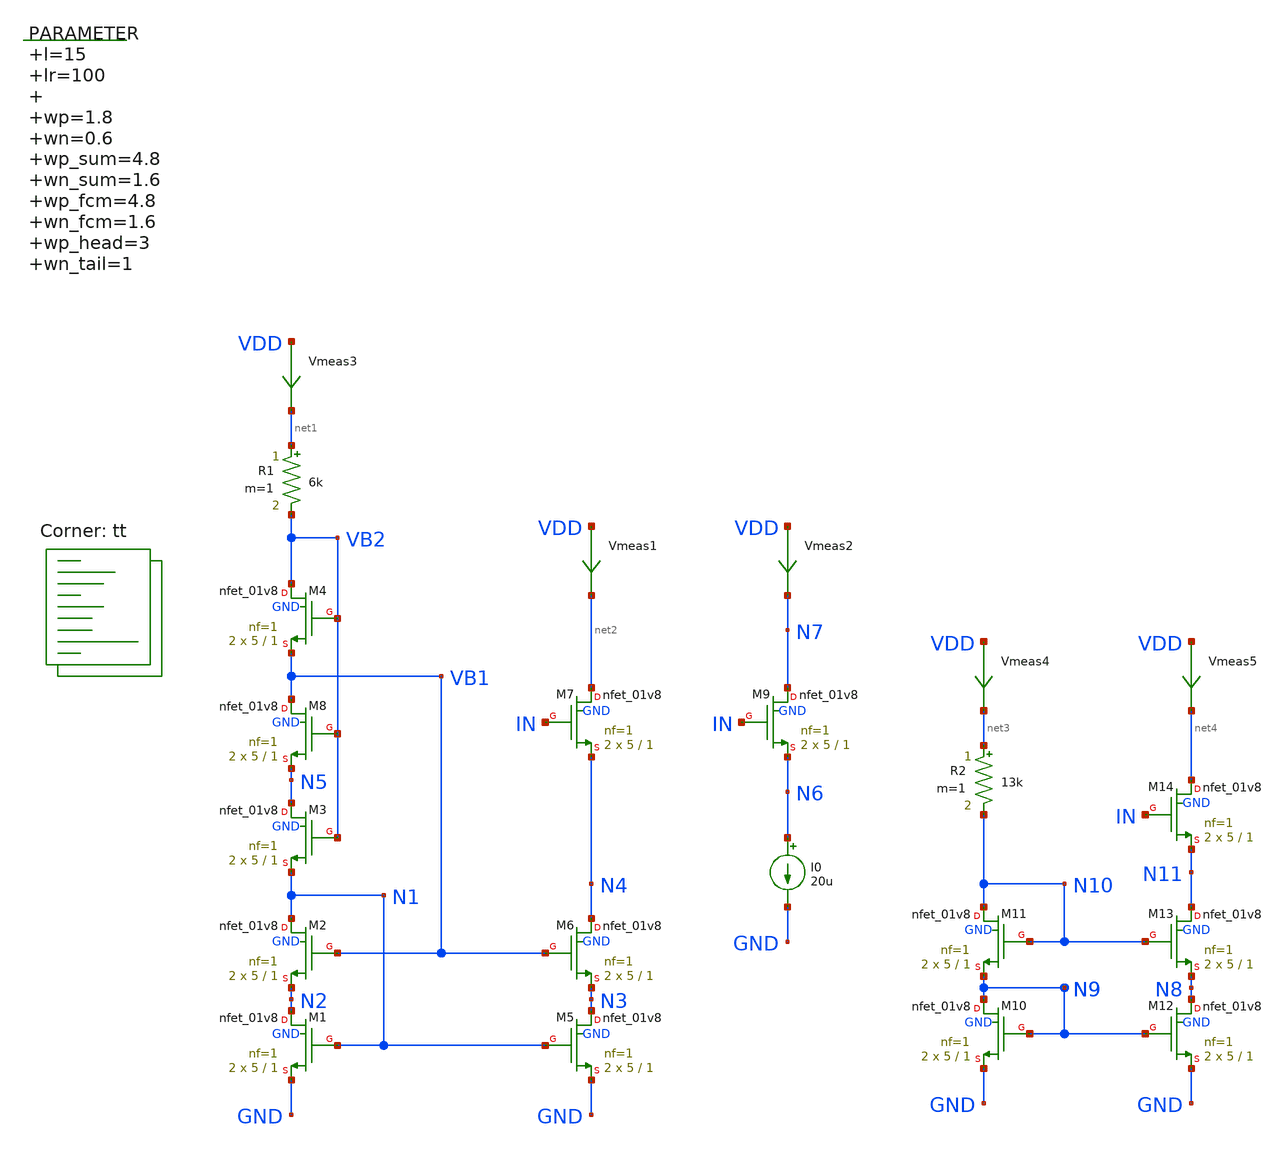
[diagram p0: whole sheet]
** sch_path: xschem/current_mirror_characterization2-tb.sch
**.subckt current_mirror_characterization2-tb
.param l=15 lr=100 wp=1.8 wn=0.6 wp_sum=4.8 wn_sum=1.6 wp_fcm=4.8 wn_fcm=1.6 wp_head=3 wn_tail=1
+ wp_bsum=4.8 wn_bsum=1.6 m=10 m1=5 m_sum=2 m_refsum=5 m_fcm=2 mdiff0=2
Vmeas3 VDD net1 0
.save i(vmeas3)
XM1 N2 N1 GND GND sky130_fd_pr__nfet_01v8 L=1 W=5 nf=1 ad='int((nf+1)/2) * W/nf * 0.29' as='int((nf+2)/2) * W/nf * 0.29'
+ pd='2*int((nf+1)/2) * (W/nf + 0.29)' ps='2*int((nf+2)/2) * (W/nf + 0.29)' nrd='0.29 / W' nrs='0.29 / W'
+ sa=0 sb=0 sd=0 mult=2 m=2
R1 net1 VB2 6k m=1
XM2 N1 VB1 N2 GND sky130_fd_pr__nfet_01v8 L=1 W=5 nf=1 ad='int((nf+1)/2) * W/nf * 0.29' as='int((nf+2)/2) * W/nf * 0.29'
+ pd='2*int((nf+1)/2) * (W/nf + 0.29)' ps='2*int((nf+2)/2) * (W/nf + 0.29)' nrd='0.29 / W' nrs='0.29 / W'
+ sa=0 sb=0 sd=0 mult=2 m=2
XM3 N5 VB2 N1 GND sky130_fd_pr__nfet_01v8 L=1 W=5 nf=1 ad='int((nf+1)/2) * W/nf * 0.29' as='int((nf+2)/2) * W/nf * 0.29'
+ pd='2*int((nf+1)/2) * (W/nf + 0.29)' ps='2*int((nf+2)/2) * (W/nf + 0.29)' nrd='0.29 / W' nrs='0.29 / W'
+ sa=0 sb=0 sd=0 mult=2 m=2
XM4 VB2 VB2 VB1 GND sky130_fd_pr__nfet_01v8 L=1 W=5 nf=1 ad='int((nf+1)/2) * W/nf * 0.29' as='int((nf+2)/2) * W/nf * 0.29'
+ pd='2*int((nf+1)/2) * (W/nf + 0.29)' ps='2*int((nf+2)/2) * (W/nf + 0.29)' nrd='0.29 / W' nrs='0.29 / W'
+ sa=0 sb=0 sd=0 mult=2 m=2
XM5 N3 N1 GND GND sky130_fd_pr__nfet_01v8 L=1 W=5 nf=1 ad='int((nf+1)/2) * W/nf * 0.29' as='int((nf+2)/2) * W/nf * 0.29'
+ pd='2*int((nf+1)/2) * (W/nf + 0.29)' ps='2*int((nf+2)/2) * (W/nf + 0.29)' nrd='0.29 / W' nrs='0.29 / W'
+ sa=0 sb=0 sd=0 mult=2 m=2
XM6 N4 VB1 N3 GND sky130_fd_pr__nfet_01v8 L=1 W=5 nf=1 ad='int((nf+1)/2) * W/nf * 0.29' as='int((nf+2)/2) * W/nf * 0.29'
+ pd='2*int((nf+1)/2) * (W/nf + 0.29)' ps='2*int((nf+2)/2) * (W/nf + 0.29)' nrd='0.29 / W' nrs='0.29 / W'
+ sa=0 sb=0 sd=0 mult=2 m=2
Vmeas1 VDD net2 0
.save i(vmeas1)
XM8 VB1 VB2 N5 GND sky130_fd_pr__nfet_01v8 L=1 W=5 nf=1 ad='int((nf+1)/2) * W/nf * 0.29' as='int((nf+2)/2) * W/nf * 0.29'
+ pd='2*int((nf+1)/2) * (W/nf + 0.29)' ps='2*int((nf+2)/2) * (W/nf + 0.29)' nrd='0.29 / W' nrs='0.29 / W'
+ sa=0 sb=0 sd=0 mult=2 m=2
XM7 net2 IN N4 GND sky130_fd_pr__nfet_01v8 L=1 W=5 nf=1 ad='int((nf+1)/2) * W/nf * 0.29' as='int((nf+2)/2) * W/nf * 0.29'
+ pd='2*int((nf+1)/2) * (W/nf + 0.29)' ps='2*int((nf+2)/2) * (W/nf + 0.29)' nrd='0.29 / W' nrs='0.29 / W'
+ sa=0 sb=0 sd=0 mult=2 m=2
Vmeas2 VDD N7 0
.save i(vmeas2)
XM9 N7 IN N6 GND sky130_fd_pr__nfet_01v8 L=1 W=5 nf=1 ad='int((nf+1)/2) * W/nf * 0.29' as='int((nf+2)/2) * W/nf * 0.29'
+ pd='2*int((nf+1)/2) * (W/nf + 0.29)' ps='2*int((nf+2)/2) * (W/nf + 0.29)' nrd='0.29 / W' nrs='0.29 / W'
+ sa=0 sb=0 sd=0 mult=2 m=2
I0 N6 GND 20u
XM10 N9 N9 GND GND sky130_fd_pr__nfet_01v8 L=1 W=5 nf=1 ad='int((nf+1)/2) * W/nf * 0.29' as='int((nf+2)/2) * W/nf * 0.29'
+ pd='2*int((nf+1)/2) * (W/nf + 0.29)' ps='2*int((nf+2)/2) * (W/nf + 0.29)' nrd='0.29 / W' nrs='0.29 / W'
+ sa=0 sb=0 sd=0 mult=2 m=2
XM11 N10 N10 N9 GND sky130_fd_pr__nfet_01v8 L=1 W=5 nf=1 ad='int((nf+1)/2) * W/nf * 0.29' as='int((nf+2)/2) * W/nf * 0.29'
+ pd='2*int((nf+1)/2) * (W/nf + 0.29)' ps='2*int((nf+2)/2) * (W/nf + 0.29)' nrd='0.29 / W' nrs='0.29 / W'
+ sa=0 sb=0 sd=0 mult=2 m=2
Vmeas4 VDD net3 0
.save i(vmeas4)
R2 net3 N10 13k m=1
XM12 N8 N9 GND GND sky130_fd_pr__nfet_01v8 L=1 W=5 nf=1 ad='int((nf+1)/2) * W/nf * 0.29' as='int((nf+2)/2) * W/nf * 0.29'
+ pd='2*int((nf+1)/2) * (W/nf + 0.29)' ps='2*int((nf+2)/2) * (W/nf + 0.29)' nrd='0.29 / W' nrs='0.29 / W'
+ sa=0 sb=0 sd=0 mult=2 m=2
XM13 N11 N10 N8 GND sky130_fd_pr__nfet_01v8 L=1 W=5 nf=1 ad='int((nf+1)/2) * W/nf * 0.29' as='int((nf+2)/2) * W/nf * 0.29'
+ pd='2*int((nf+1)/2) * (W/nf + 0.29)' ps='2*int((nf+2)/2) * (W/nf + 0.29)' nrd='0.29 / W' nrs='0.29 / W'
+ sa=0 sb=0 sd=0 mult=2 m=2
XM14 net4 IN N11 GND sky130_fd_pr__nfet_01v8 L=1 W=5 nf=1 ad='int((nf+1)/2) * W/nf * 0.29' as='int((nf+2)/2) * W/nf * 0.29'
+ pd='2*int((nf+1)/2) * (W/nf + 0.29)' ps='2*int((nf+2)/2) * (W/nf + 0.29)' nrd='0.29 / W' nrs='0.29 / W'
+ sa=0 sb=0 sd=0 mult=2 m=2
Vmeas5 VDD net4 0
.save i(vmeas5)
**** begin user architecture code
.lib $::SKYWATER_MODELS/sky130.lib.spice tt



  .option wnflag=1
  .option safecurrents
  ********************Static Current Sources***************************
  .param iref=10u
  *Iref n4 gnd 100n
  ********************Static Voltage Sources***************************
  Vdd vdd gnd dc 1.8
  VIN IN gnd dc 0
  *VB1 VB1 gnd 0
  ********************Simulation Commands*****************************
  .control
     reset
     save all
     *tran 0.1p 300p
     dc VIN 0 1.8 0.01
     *dc R2 1k 100k 1k
     write current_mirror2-tb.raw
     set appendwrite
*    quit 0
  .endc



**** end user architecture code
**.ends
.end
